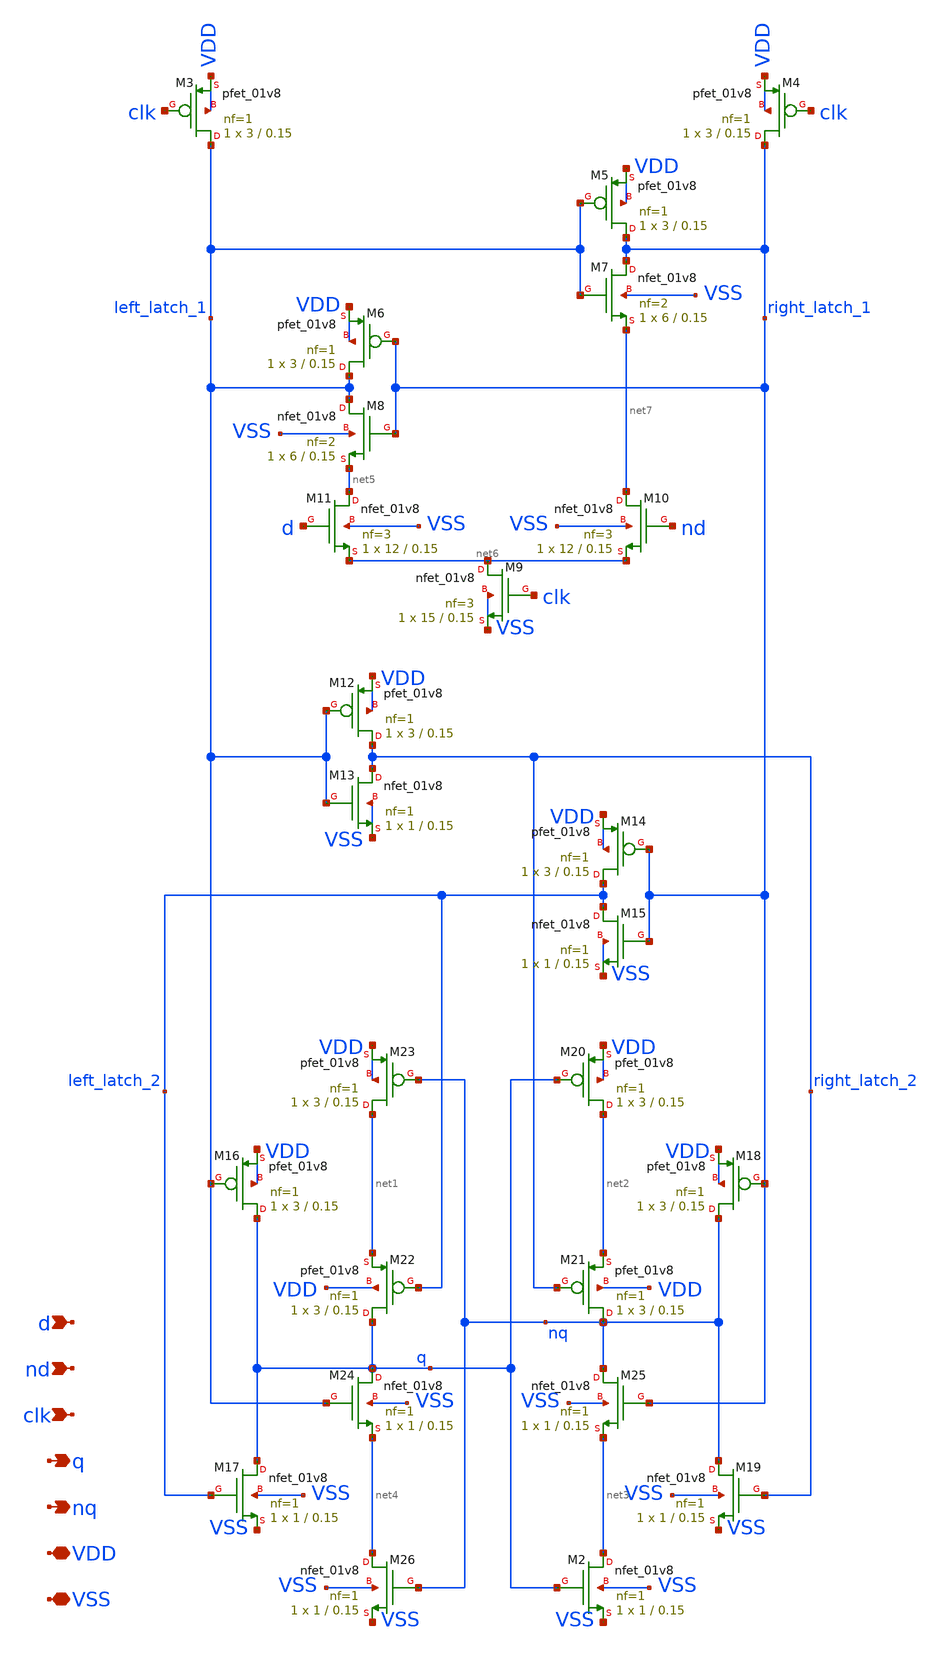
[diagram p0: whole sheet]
** sch_path: tt_um_13hihi31_tdc/xschem/saff.sch
**.subckt saff VDD d q VSS nd clk nq
*.iopin VDD
*.ipin d
*.opin q
*.iopin VSS
*.ipin nd
*.ipin clk
*.opin nq
XM2 net3 q VSS VSS sky130_fd_pr__nfet_01v8 L=0.15 W=1 nf=1 ad='int((nf+1)/2) * W/nf * 0.29' as='int((nf+2)/2) * W/nf * 0.29'
+ pd='2*int((nf+1)/2) * (W/nf + 0.29)' ps='2*int((nf+2)/2) * (W/nf + 0.29)' nrd='0.29 / W' nrs='0.29 / W'
+ sa=0 sb=0 sd=0 mult=1 m=1
XM3 left_latch_1 clk VDD VDD sky130_fd_pr__pfet_01v8 L=0.15 W=3 nf=1 ad='int((nf+1)/2) * W/nf * 0.29'
+ as='int((nf+2)/2) * W/nf * 0.29' pd='2*int((nf+1)/2) * (W/nf + 0.29)' ps='2*int((nf+2)/2) * (W/nf + 0.29)'
+ nrd='0.29 / W' nrs='0.29 / W' sa=0 sb=0 sd=0 mult=1 m=1
XM4 right_latch_1 clk VDD VDD sky130_fd_pr__pfet_01v8 L=0.15 W=3 nf=1 ad='int((nf+1)/2) * W/nf * 0.29'
+ as='int((nf+2)/2) * W/nf * 0.29' pd='2*int((nf+1)/2) * (W/nf + 0.29)' ps='2*int((nf+2)/2) * (W/nf + 0.29)'
+ nrd='0.29 / W' nrs='0.29 / W' sa=0 sb=0 sd=0 mult=1 m=1
XM5 right_latch_1 left_latch_1 VDD VDD sky130_fd_pr__pfet_01v8 L=0.15 W=3 nf=1 ad='int((nf+1)/2) * W/nf * 0.29'
+ as='int((nf+2)/2) * W/nf * 0.29' pd='2*int((nf+1)/2) * (W/nf + 0.29)' ps='2*int((nf+2)/2) * (W/nf + 0.29)'
+ nrd='0.29 / W' nrs='0.29 / W' sa=0 sb=0 sd=0 mult=1 m=1
XM6 left_latch_1 right_latch_1 VDD VDD sky130_fd_pr__pfet_01v8 L=0.15 W=3 nf=1 ad='int((nf+1)/2) * W/nf * 0.29'
+ as='int((nf+2)/2) * W/nf * 0.29' pd='2*int((nf+1)/2) * (W/nf + 0.29)' ps='2*int((nf+2)/2) * (W/nf + 0.29)'
+ nrd='0.29 / W' nrs='0.29 / W' sa=0 sb=0 sd=0 mult=1 m=1
XM7 right_latch_1 left_latch_1 net7 VSS sky130_fd_pr__nfet_01v8 L=0.15 W=6 nf=2 ad='int((nf+1)/2) * W/nf * 0.29'
+ as='int((nf+2)/2) * W/nf * 0.29' pd='2*int((nf+1)/2) * (W/nf + 0.29)' ps='2*int((nf+2)/2) * (W/nf + 0.29)'
+ nrd='0.29 / W' nrs='0.29 / W' sa=0 sb=0 sd=0 mult=1 m=1
XM8 left_latch_1 right_latch_1 net5 VSS sky130_fd_pr__nfet_01v8 L=0.15 W=6 nf=2 ad='int((nf+1)/2) * W/nf * 0.29'
+ as='int((nf+2)/2) * W/nf * 0.29' pd='2*int((nf+1)/2) * (W/nf + 0.29)' ps='2*int((nf+2)/2) * (W/nf + 0.29)'
+ nrd='0.29 / W' nrs='0.29 / W' sa=0 sb=0 sd=0 mult=1 m=1
XM9 net6 clk VSS VSS sky130_fd_pr__nfet_01v8 L=0.15 W=15 nf=3 ad='int((nf+1)/2) * W/nf * 0.29' as='int((nf+2)/2) * W/nf * 0.29'
+ pd='2*int((nf+1)/2) * (W/nf + 0.29)' ps='2*int((nf+2)/2) * (W/nf + 0.29)' nrd='0.29 / W' nrs='0.29 / W'
+ sa=0 sb=0 sd=0 mult=1 m=1
XM10 net7 nd net6 VSS sky130_fd_pr__nfet_01v8 L=0.15 W=12 nf=3 ad='int((nf+1)/2) * W/nf * 0.29' as='int((nf+2)/2) * W/nf * 0.29'
+ pd='2*int((nf+1)/2) * (W/nf + 0.29)' ps='2*int((nf+2)/2) * (W/nf + 0.29)' nrd='0.29 / W' nrs='0.29 / W'
+ sa=0 sb=0 sd=0 mult=1 m=1
XM11 net5 d net6 VSS sky130_fd_pr__nfet_01v8 L=0.15 W=12 nf=3 ad='int((nf+1)/2) * W/nf * 0.29' as='int((nf+2)/2) * W/nf * 0.29'
+ pd='2*int((nf+1)/2) * (W/nf + 0.29)' ps='2*int((nf+2)/2) * (W/nf + 0.29)' nrd='0.29 / W' nrs='0.29 / W'
+ sa=0 sb=0 sd=0 mult=1 m=1
XM12 right_latch_2 left_latch_1 VDD VDD sky130_fd_pr__pfet_01v8 L=0.15 W=3 nf=1 ad='int((nf+1)/2) * W/nf * 0.29'
+ as='int((nf+2)/2) * W/nf * 0.29' pd='2*int((nf+1)/2) * (W/nf + 0.29)' ps='2*int((nf+2)/2) * (W/nf + 0.29)'
+ nrd='0.29 / W' nrs='0.29 / W' sa=0 sb=0 sd=0 mult=1 m=1
XM13 right_latch_2 left_latch_1 VSS VSS sky130_fd_pr__nfet_01v8 L=0.15 W=1 nf=1 ad='int((nf+1)/2) * W/nf * 0.29'
+ as='int((nf+2)/2) * W/nf * 0.29' pd='2*int((nf+1)/2) * (W/nf + 0.29)' ps='2*int((nf+2)/2) * (W/nf + 0.29)'
+ nrd='0.29 / W' nrs='0.29 / W' sa=0 sb=0 sd=0 mult=1 m=1
XM14 left_latch_2 right_latch_1 VDD VDD sky130_fd_pr__pfet_01v8 L=0.15 W=3 nf=1 ad='int((nf+1)/2) * W/nf * 0.29'
+ as='int((nf+2)/2) * W/nf * 0.29' pd='2*int((nf+1)/2) * (W/nf + 0.29)' ps='2*int((nf+2)/2) * (W/nf + 0.29)'
+ nrd='0.29 / W' nrs='0.29 / W' sa=0 sb=0 sd=0 mult=1 m=1
XM15 left_latch_2 right_latch_1 VSS VSS sky130_fd_pr__nfet_01v8 L=0.15 W=1 nf=1 ad='int((nf+1)/2) * W/nf * 0.29'
+ as='int((nf+2)/2) * W/nf * 0.29' pd='2*int((nf+1)/2) * (W/nf + 0.29)' ps='2*int((nf+2)/2) * (W/nf + 0.29)'
+ nrd='0.29 / W' nrs='0.29 / W' sa=0 sb=0 sd=0 mult=1 m=1
XM16 q left_latch_1 VDD VDD sky130_fd_pr__pfet_01v8 L=0.15 W=3 nf=1 ad='int((nf+1)/2) * W/nf * 0.29'
+ as='int((nf+2)/2) * W/nf * 0.29' pd='2*int((nf+1)/2) * (W/nf + 0.29)' ps='2*int((nf+2)/2) * (W/nf + 0.29)'
+ nrd='0.29 / W' nrs='0.29 / W' sa=0 sb=0 sd=0 mult=1 m=1
XM17 q left_latch_2 VSS VSS sky130_fd_pr__nfet_01v8 L=0.15 W=1 nf=1 ad='int((nf+1)/2) * W/nf * 0.29'
+ as='int((nf+2)/2) * W/nf * 0.29' pd='2*int((nf+1)/2) * (W/nf + 0.29)' ps='2*int((nf+2)/2) * (W/nf + 0.29)'
+ nrd='0.29 / W' nrs='0.29 / W' sa=0 sb=0 sd=0 mult=1 m=1
XM18 nq right_latch_1 VDD VDD sky130_fd_pr__pfet_01v8 L=0.15 W=3 nf=1 ad='int((nf+1)/2) * W/nf * 0.29'
+ as='int((nf+2)/2) * W/nf * 0.29' pd='2*int((nf+1)/2) * (W/nf + 0.29)' ps='2*int((nf+2)/2) * (W/nf + 0.29)'
+ nrd='0.29 / W' nrs='0.29 / W' sa=0 sb=0 sd=0 mult=1 m=1
XM19 nq right_latch_2 VSS VSS sky130_fd_pr__nfet_01v8 L=0.15 W=1 nf=1 ad='int((nf+1)/2) * W/nf * 0.29'
+ as='int((nf+2)/2) * W/nf * 0.29' pd='2*int((nf+1)/2) * (W/nf + 0.29)' ps='2*int((nf+2)/2) * (W/nf + 0.29)'
+ nrd='0.29 / W' nrs='0.29 / W' sa=0 sb=0 sd=0 mult=1 m=1
XM20 net2 q VDD VDD sky130_fd_pr__pfet_01v8 L=0.15 W=3 nf=1 ad='int((nf+1)/2) * W/nf * 0.29' as='int((nf+2)/2) * W/nf * 0.29'
+ pd='2*int((nf+1)/2) * (W/nf + 0.29)' ps='2*int((nf+2)/2) * (W/nf + 0.29)' nrd='0.29 / W' nrs='0.29 / W'
+ sa=0 sb=0 sd=0 mult=1 m=1
XM21 nq right_latch_2 net2 VDD sky130_fd_pr__pfet_01v8 L=0.15 W=3 nf=1 ad='int((nf+1)/2) * W/nf * 0.29'
+ as='int((nf+2)/2) * W/nf * 0.29' pd='2*int((nf+1)/2) * (W/nf + 0.29)' ps='2*int((nf+2)/2) * (W/nf + 0.29)'
+ nrd='0.29 / W' nrs='0.29 / W' sa=0 sb=0 sd=0 mult=1 m=1
XM22 q left_latch_2 net1 VDD sky130_fd_pr__pfet_01v8 L=0.15 W=3 nf=1 ad='int((nf+1)/2) * W/nf * 0.29'
+ as='int((nf+2)/2) * W/nf * 0.29' pd='2*int((nf+1)/2) * (W/nf + 0.29)' ps='2*int((nf+2)/2) * (W/nf + 0.29)'
+ nrd='0.29 / W' nrs='0.29 / W' sa=0 sb=0 sd=0 mult=1 m=1
XM23 net1 nq VDD VDD sky130_fd_pr__pfet_01v8 L=0.15 W=3 nf=1 ad='int((nf+1)/2) * W/nf * 0.29' as='int((nf+2)/2) * W/nf * 0.29'
+ pd='2*int((nf+1)/2) * (W/nf + 0.29)' ps='2*int((nf+2)/2) * (W/nf + 0.29)' nrd='0.29 / W' nrs='0.29 / W'
+ sa=0 sb=0 sd=0 mult=1 m=1
XM24 q left_latch_1 net4 VSS sky130_fd_pr__nfet_01v8 L=0.15 W=1 nf=1 ad='int((nf+1)/2) * W/nf * 0.29'
+ as='int((nf+2)/2) * W/nf * 0.29' pd='2*int((nf+1)/2) * (W/nf + 0.29)' ps='2*int((nf+2)/2) * (W/nf + 0.29)'
+ nrd='0.29 / W' nrs='0.29 / W' sa=0 sb=0 sd=0 mult=1 m=1
XM25 nq right_latch_1 net3 VSS sky130_fd_pr__nfet_01v8 L=0.15 W=1 nf=1 ad='int((nf+1)/2) * W/nf * 0.29'
+ as='int((nf+2)/2) * W/nf * 0.29' pd='2*int((nf+1)/2) * (W/nf + 0.29)' ps='2*int((nf+2)/2) * (W/nf + 0.29)'
+ nrd='0.29 / W' nrs='0.29 / W' sa=0 sb=0 sd=0 mult=1 m=1
XM26 net4 nq VSS VSS sky130_fd_pr__nfet_01v8 L=0.15 W=1 nf=1 ad='int((nf+1)/2) * W/nf * 0.29' as='int((nf+2)/2) * W/nf * 0.29'
+ pd='2*int((nf+1)/2) * (W/nf + 0.29)' ps='2*int((nf+2)/2) * (W/nf + 0.29)' nrd='0.29 / W' nrs='0.29 / W'
+ sa=0 sb=0 sd=0 mult=1 m=1
**.ends
.end
